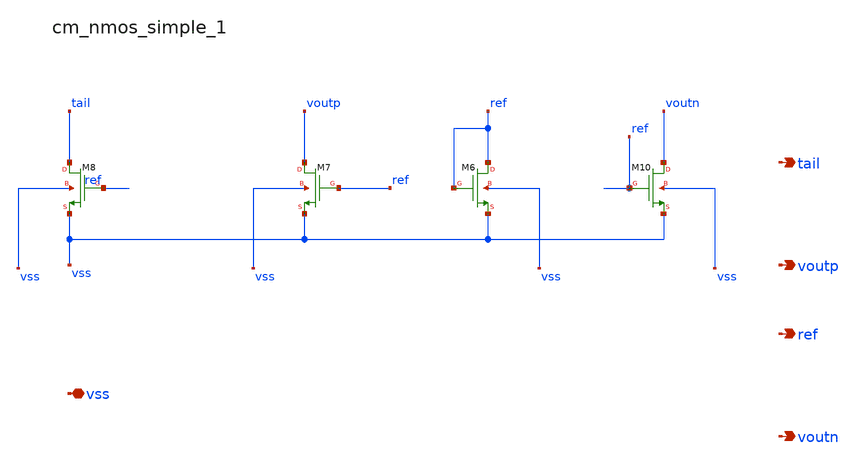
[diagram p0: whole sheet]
** sch_path: analog-db/raw/amp_020_two_stage_miller_cmfb/hier/blocks/cm_nmos_simple_1.sch
**.subckt cm_nmos_simple_1 vss tail voutp ref voutn
*.iopin vss
*.opin tail
*.opin voutp
*.opin ref
*.opin voutn
XM10 voutn ref vss vss sg13_lv_nmos w=x_dut_xm10_w l=x_dut_xm10_l ng=1 m=x_dut_xm10_m
XM6 ref ref vss vss sg13_lv_nmos w=x_dut_xm6_w l=x_dut_xm6_l ng=1 m=x_dut_xm6_m
XM7 voutp ref vss vss sg13_lv_nmos w=x_dut_xm7_w l=x_dut_xm7_l ng=1 m=x_dut_xm7_m
XM8 tail ref vss vss sg13_lv_nmos w=x_dut_xm8_w l=x_dut_xm8_l ng=1 m=x_dut_xm8_m
**.ends
.end
